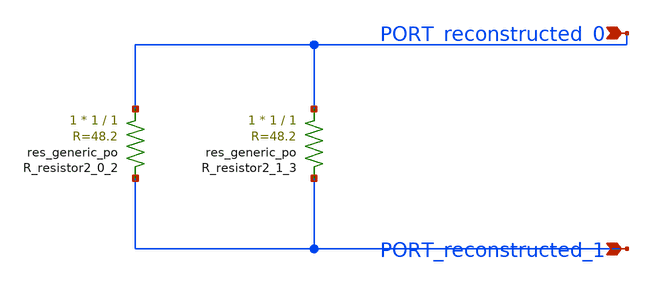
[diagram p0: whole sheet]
** sch_path: schematics/AMSNet/431.sch
**.subckt 431 PORT_reconstructed_0 PORT_reconstructed_1
*.ipin PORT_reconstructed_0
*.ipin PORT_reconstructed_1
XR_resistor2_0_2 PORT_reconstructed_0 PORT_reconstructed_1 sky130_fd_pr__res_generic_po W=1 L=1 m=1
XR_resistor2_1_3 PORT_reconstructed_0 PORT_reconstructed_1 sky130_fd_pr__res_generic_po W=1 L=1 m=1
**.ends
.end
